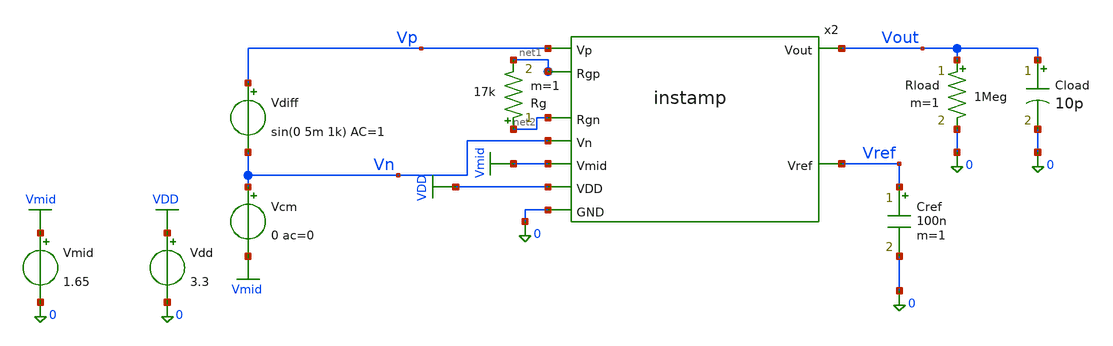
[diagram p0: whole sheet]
** sch_path: xschem/instamp_tb.sch
* Copyright 2021 Stefan Frederik Schippers
* Licensed under the Apache License, Version 2.0 (the "License");
* you may not use this file except in compliance with the License.
* You may obtain a copy of the License at
* https://www.apache.org/licenses/LICENSE-2.0
* Unless required by applicable law or agreed to in writing, software
* distributed under the License is distributed on an "AS IS" BASIS,
* WITHOUT WARRANTIES OR CONDITIONS OF ANY KIND, either express or implied.
* See the License for the specific language governing permissions and
* limitations under the License.
**.subckt instamp_tb
Vdd VDD 0 3.3
Vdiff Vp Vn sin(0 5m 1k) AC=1
Vmid Vmid 0 1.65
Vcm Vn Vmid 0 ac=0
x2 Vn net2 Vp net1 Vmid Vout Vref VDD 0 instamp
Cref Vref 0 100n m=1
Rg net2 net1 17k m=1
Rload Vout 0 1Meg m=1
Cload Vout 0 10p m=1
**** begin user architecture code

** opencircuitdesign pdks install
.lib $::SKYWATER_MODELS/sky130.lib.spice tt



.option wnflag=1
.option savecurrents
.option rshunt=1e12

# if one of these is uncommented, it will
# override the subcircuit in the symbol
# from the cace extracction
#.include ../netlist/rcx/instamp.spice
# from the mag extraction
#.include ../netlist/layout/instamp.spice

.save all
.control
if 0
op
write instamp_tb.raw
endif

set appendwrite
set gnuplot_terminal=png/quit

* write instamp_tb.raw
if 0
* differential gain tran
  destroy all
  foreach val 10k 5k 1k
    alter Rg = $val
    tran 10u 3m 1m
  end
  let Rg10k = tran1.v(vout)
  let Rg5k = tran2.v(vout)
  let Rg1k = tran3.v(vout)
  gnuplot tran Rg10k Rg5k Rg1k
*+ title 'Differential gain'  xlabel 'Time' ylabel 'Volts'
endif

# rise and fall times
if 0
let per=5u
let tstop=$&per*3
let tstep=per/1000
alter Rg=90k
alter @Vdiff[pulse] [ 0 100m $&per 1n 1n $&per $&tstop ]
tran $&tstep $&tstop
plot V(Vp,vmid) V(vout,vmid)
meas tran v_min MIN V(Vout)
meas tran v_pp PP V(Vout)
let v_high=(0.9*v_pp)+v_min
let v_low=(0.1*v_pp)+v_min
meas tran rise_time TRIG v(Vout) VAL='v_low' rise=1 targ v(vout) Val='v_high' RISE=1
let sr=(v_high-v_low)/rise_time
print sr

  gnuplot v_rise_fall V(vp,vmid) V(Vout,vmid)  title 'Rise and Fall Times'  xlabel 'Time (s)' ylabel
+ 'Volts'

endif

if 0
ac dec 100 1 1Meg
let gain = db(V(Vout))
let cutoff_db = vecmax(gain)-3.0
meas ac bw WHEN gain=cutoff_db FALL =1
meas ac max_gain MAX gain
print bw max_gain
endif
* run ac on schematic as drawn
if 1
  destroy all
* differential gain ac
  ac dec 100 1 1Meg
  plot db(v(vout))
endif

* run ac cmrr and psrr sweeps
if 0
  destroy all
* differential gain ac
  alter vdiff ac=1
  alter vcm ac=0
  alter vdd ac=0
  foreach val 10k 5k 1k
    alter Rg = $val
    ac dec 100 1 1Meg
  end
  alter vdiff ac=0
  alter vcm ac=1
  alter vdd ac=0
  foreach val 10k 5k 1k
    alter Rg = $val
    ac dec 100 1 1Meg
  end
  alter vdiff ac=0
  alter vcm ac=0
  alter vdd ac=1
  foreach val 10k 5k 1k
    alter Rg = $val
    ac dec 100 1 1Meg
  end
  alter vdiff ac=0
  alter vcm ac=0
  alter vdd ac=0
  alter vmid ac=1
  foreach val 10k 5k 1k
    alter Rg = $val
    ac dec 100 1 1Meg
  end
  let Rg10k = db(ac1.v(vout))
  let Rg5k = db(ac2.v(vout))
  let Rg1k = db(ac3.v(vout))
  let Rg10k_cm = Rg10k-db(ac4.v(vout))
  let Rg5k_cm = Rg5k-db(ac5.v(vout))
  let Rg1k_cm = Rg1k-db(ac6.v(vout))
  let Rg10k_psh = Rg10k-db(ac7.v(vout))
  let Rg5k_psh = Rg5k-db(ac8.v(vout))
  let Rg1k_psh = Rg1k-db(ac9.v(vout))
  let Rg10k_vmid = Rg10k-db(ac10.v(vout))
  let Rg5k_vmid = Rg5k-db(ac11.v(vout))
  let Rg1k_vmid = Rg1k-db(ac12.v(vout))

  gnuplot ac Rg10k Rg5k Rg1k  title 'Differential gain'  xlabel 'Freq' ylabel 'Gain dB'
  gnuplot cmrr Rg10k_cm Rg5k_cm Rg1k_cm  title 'CMRR'  xlabel 'Freq' ylabel 'Gain dB'
  gnuplot psrr Rg10k_psh Rg5k_psh Rg1k_psh  title 'PSRR'  xlabel 'Freq' ylabel 'Gain dB'
  gnuplot vmid_rej Rg10k_vmid Rg5k_vmid Rg1k_vmid  title 'Vmid Rejection'  xlabel 'Freq' ylabel 'Gain dB'

endif

if 0
* common mode gain
  alter vdiff ac=0
  alter vcm ac=1
  foreach val 90k 5k 1k
    alter Rg = $val
    ac dec 100 1 10Meg
  end

  plot db(ac1.V(Vout)) db(ac2.V(Vout))   db(ac3.V(Vout)) title 'Mag Vout'

* power supply gain
  alter vcm ac=0
  alter vdd ac=1
  foreach val 90k 5k 1k
    alter Rg = $val
    ac dec 100 1 10Meg
  end

  plot db(ac4.V(Vout)) db(ac5.V(Vout))   db(ac6.V(Vout)) title 'Mag Vout'

endif

.endc


**** end user architecture code
**.ends

* expanding   symbol:  instamp.sym # of pins=9
** sym_path: xschem/instamp.sym
** sch_path: xschem/instamp.sch
.subckt instamp Vn Rgn Vp Rgp Vmid Vout Vref VDD GND
*.ipin Vp
*.ipin Vn
*.opin Vout
*.opin Vref
*.ipin Rgp
*.ipin Rgn
*.ipin Vmid
*.ipin GND
*.ipin VDD
XR1 Rgp Vout3 GND sky130_fd_pr__res_high_po_0p35 L=76.36 mult=1 m=1
XR2 Rgn Vout2 GND sky130_fd_pr__res_high_po_0p35 L=76.36 mult=1 m=1
XR3 Vout2 Vn4 GND sky130_fd_pr__res_high_po_0p35 L=51.36 mult=1 m=1
XR4 Vout3 Vp4 GND sky130_fd_pr__res_high_po_0p35 L=51.36 mult=1 m=1
XR5 Vp4 Vout5 GND sky130_fd_pr__res_high_po_0p35 L=51.36 mult=1 m=1
XR6 Vn4 Vout GND sky130_fd_pr__res_high_po_0p35 L=51.36 mult=1 m=1
x6 Vref Vout3 Vp Rgp VDD GND opamp
x2 Vref Vout2 Vn Rgn VDD GND opamp
x3 Vref Vout Vp4 Vn4 VDD GND opamp
x4 Vref Vout5 Vmid Vout5 VDD GND opamp
x1 Vref GND VDD bandgap
.ends


* expanding   symbol:  opamp.sym # of pins=6
** sym_path: xschem/opamp.sym
** sch_path: xschem/opamp.sch
.subckt opamp Vref Vout Vp Vn VDD GND
*.opin Vout
*.ipin Vref
*.ipin Vp
*.ipin Vn
*.ipin GND
*.ipin VDD
XM1 Vg1 Vg1 net1 GND sky130_fd_pr__nfet_g5v0d10v5 L=2 W=3.33 nf=1 ad='int((1 + 1)/2) * 3.33 / 1 * 0.29'
+ as='int((1 + 2)/2) * 3.33 / 1 * 0.29' pd='2*int((1 + 1)/2) * (3.33 / 1 + 0.29)' ps='2*int((1 + 2)/2) * (3.33 / 1 + 0.29)'
+ nrd='0.29 / 3.33 ' nrs='0.29 / 3.33 ' sa=0 sb=0 sd=0 mult=3 m=3
XM2 net1 Vg1 GND GND sky130_fd_pr__nfet_g5v0d10v5 L=5 W=5 nf=1 ad='int((1 + 1)/2) * 5 / 1 * 0.29' as='int((1 + 2)/2) * 5 / 1 * 0.29'
+ pd='2*int((1 + 1)/2) * (5 / 1 + 0.29)' ps='2*int((1 + 2)/2) * (5 / 1 + 0.29)' nrd='0.29 / 5 ' nrs='0.29 / 5 '
+ sa=0 sb=0 sd=0 mult=1 m=1
XM4 net2 Vg1 GND GND sky130_fd_pr__nfet_g5v0d10v5 L=5 W=5 nf=1 ad='int((1 + 1)/2) * 5 / 1 * 0.29' as='int((1 + 2)/2) * 5 / 1 * 0.29'
+ pd='2*int((1 + 1)/2) * (5 / 1 + 0.29)' ps='2*int((1 + 2)/2) * (5 / 1 + 0.29)' nrd='0.29 / 5 ' nrs='0.29 / 5 '
+ sa=0 sb=0 sd=0 mult=1 m=1
XM3 Vg5 Vg1 net2 GND sky130_fd_pr__nfet_g5v0d10v5 L=2 W=3.33 nf=1 ad='int((1 + 1)/2) * 3.33 / 1 * 0.29'
+ as='int((1 + 2)/2) * 3.33 / 1 * 0.29' pd='2*int((1 + 1)/2) * (3.33 / 1 + 0.29)' ps='2*int((1 + 2)/2) * (3.33 / 1 + 0.29)'
+ nrd='0.29 / 3.33 ' nrs='0.29 / 3.33 ' sa=0 sb=0 sd=0 mult=3 m=3
XMr1 net6 Vref GND GND sky130_fd_pr__nfet_g5v0d10v5 L=8 W=5 nf=1 ad='int((1 + 1)/2) * 5 / 1 * 0.29' as='int((1 + 2)/2) * 5 / 1 * 0.29'
+ pd='2*int((1 + 1)/2) * (5 / 1 + 0.29)' ps='2*int((1 + 2)/2) * (5 / 1 + 0.29)' nrd='0.29 / 5 ' nrs='0.29 / 5 '
+ sa=0 sb=0 sd=0 mult=1 m=1
XMr2 VgR2 VgR2 VDD VDD sky130_fd_pr__pfet_g5v0d10v5 L=5 W=4 nf=1 ad='int((1 + 1)/2) * 4 / 1 * 0.29' as='int((1 + 2)/2) * 4 / 1 * 0.29'
+ pd='2*int((1 + 1)/2) * (4 / 1 + 0.29)' ps='2*int((1 + 2)/2) * (4 / 1 + 0.29)' nrd='0.29 / 4 ' nrs='0.29 / 4 '
+ sa=0 sb=0 sd=0 mult=1 m=1
XMr3 Vg1 VgR2 VDD VDD sky130_fd_pr__pfet_g5v0d10v5 L=5 W=4 nf=1 ad='int((1 + 1)/2) * 4 / 1 * 0.29' as='int((1 + 2)/2) * 4 / 1 * 0.29'
+ pd='2*int((1 + 1)/2) * (4 / 1 + 0.29)' ps='2*int((1 + 2)/2) * (4 / 1 + 0.29)' nrd='0.29 / 4 ' nrs='0.29 / 4 '
+ sa=0 sb=0 sd=0 mult=1 m=1
XM32 net3 Vg1 GND GND sky130_fd_pr__nfet_g5v0d10v5 L=5 W=10 nf=1 ad='int((1 + 1)/2) * 10 / 1 * 0.29'
+ as='int((1 + 2)/2) * 10 / 1 * 0.29' pd='2*int((1 + 1)/2) * (10 / 1 + 0.29)' ps='2*int((1 + 2)/2) * (10 / 1 + 0.29)'
+ nrd='0.29 / 10 ' nrs='0.29 / 10 ' sa=0 sb=0 sd=0 mult=1 m=1
XM31 Vs29 Vg1 net3 GND sky130_fd_pr__nfet_g5v0d10v5 L=2 W=6.66 nf=1 ad='int((1 + 1)/2) * 6.66 / 1 * 0.29'
+ as='int((1 + 2)/2) * 6.66 / 1 * 0.29' pd='2*int((1 + 1)/2) * (6.66 / 1 + 0.29)' ps='2*int((1 + 2)/2) * (6.66 / 1 + 0.29)'
+ nrd='0.29 / 6.66 ' nrs='0.29 / 6.66 ' sa=0 sb=0 sd=0 mult=3 m=3
XM15 Vg11 Vg1 Vd10 GND sky130_fd_pr__nfet_g5v0d10v5 L=2 W=14.3 nf=1 ad='int((1 + 1)/2) * 14.3 / 1 * 0.29'
+ as='int((1 + 2)/2) * 14.3 / 1 * 0.29' pd='2*int((1 + 1)/2) * (14.3 / 1 + 0.29)' ps='2*int((1 + 2)/2) * (14.3 / 1 + 0.29)'
+ nrd='0.29 / 14.3 ' nrs='0.29 / 14.3 ' sa=0 sb=0 sd=0 mult=7 m=7
XM16 Vd10 Vg1 GND GND sky130_fd_pr__nfet_g5v0d10v5 L=5 W=10 nf=1 ad='int((1 + 1)/2) * 10 / 1 * 0.29'
+ as='int((1 + 2)/2) * 10 / 1 * 0.29' pd='2*int((1 + 1)/2) * (10 / 1 + 0.29)' ps='2*int((1 + 2)/2) * (10 / 1 + 0.29)'
+ nrd='0.29 / 10 ' nrs='0.29 / 10 ' sa=0 sb=0 sd=0 mult=1 m=1
XM18 Vd9 Vg1 GND GND sky130_fd_pr__nfet_g5v0d10v5 L=5 W=10 nf=1 ad='int((1 + 1)/2) * 10 / 1 * 0.29' as='int((1 + 2)/2) * 10 / 1 * 0.29'
+ pd='2*int((1 + 1)/2) * (10 / 1 + 0.29)' ps='2*int((1 + 2)/2) * (10 / 1 + 0.29)' nrd='0.29 / 10 ' nrs='0.29 / 10 '
+ sa=0 sb=0 sd=0 mult=1 m=1
XM17 Vg28 Vg1 Vd9 GND sky130_fd_pr__nfet_g5v0d10v5 L=2 W=14.3 nf=1 ad='int((1 + 1)/2) * 14.3 / 1 * 0.29'
+ as='int((1 + 2)/2) * 14.3 / 1 * 0.29' pd='2*int((1 + 1)/2) * (14.3 / 1 + 0.29)' ps='2*int((1 + 2)/2) * (14.3 / 1 + 0.29)'
+ nrd='0.29 / 14.3 ' nrs='0.29 / 14.3 ' sa=0 sb=0 sd=0 mult=7 m=7
XM20 Vg22 Vg1 GND GND sky130_fd_pr__nfet_g5v0d10v5 L=5 W=1.5 nf=1 ad='int((1 + 1)/2) * 1.5 / 1 * 0.29'
+ as='int((1 + 2)/2) * 1.5 / 1 * 0.29' pd='2*int((1 + 1)/2) * (1.5 / 1 + 0.29)' ps='2*int((1 + 2)/2) * (1.5 / 1 + 0.29)'
+ nrd='0.29 / 1.5 ' nrs='0.29 / 1.5 ' sa=0 sb=0 sd=0 mult=1 m=1
XM26 Vg26 Vg26 GND GND sky130_fd_pr__nfet_g5v0d10v5 L=0.5 W=5 nf=1 ad='int((1 + 1)/2) * 5 / 1 * 0.29'
+ as='int((1 + 2)/2) * 5 / 1 * 0.29' pd='2*int((1 + 1)/2) * (5 / 1 + 0.29)' ps='2*int((1 + 2)/2) * (5 / 1 + 0.29)'
+ nrd='0.29 / 5 ' nrs='0.29 / 5 ' sa=0 sb=0 sd=0 mult=5 m=5
XM25 Vd24 Vd24 Vg26 GND sky130_fd_pr__nfet_g5v0d10v5 L=0.5 W=5 nf=1 ad='int((1 + 1)/2) * 5 / 1 * 0.29'
+ as='int((1 + 2)/2) * 5 / 1 * 0.29' pd='2*int((1 + 1)/2) * (5 / 1 + 0.29)' ps='2*int((1 + 2)/2) * (5 / 1 + 0.29)'
+ nrd='0.29 / 5 ' nrs='0.29 / 5 ' sa=0 sb=0 sd=0 mult=5 m=5
XM23 Vg27 Vd24 Vg28 GND sky130_fd_pr__nfet_g5v0d10v5 L=0.5 W=10 nf=1 ad='int((1 + 1)/2) * 10 / 1 * 0.29'
+ as='int((1 + 2)/2) * 10 / 1 * 0.29' pd='2*int((1 + 1)/2) * (10 / 1 + 0.29)' ps='2*int((1 + 2)/2) * (10 / 1 + 0.29)'
+ nrd='0.29 / 10 ' nrs='0.29 / 10 ' sa=0 sb=0 sd=0 mult=5 m=5
XM28 Vout Vg28 GND GND sky130_fd_pr__nfet_g5v0d10v5 L=0.5 W=10 nf=1 ad='int((1 + 1)/2) * 10 / 1 * 0.29'
+ as='int((1 + 2)/2) * 10 / 1 * 0.29' pd='2*int((1 + 1)/2) * (10 / 1 + 0.29)' ps='2*int((1 + 2)/2) * (10 / 1 + 0.29)'
+ nrd='0.29 / 10 ' nrs='0.29 / 10 ' sa=0 sb=0 sd=0 mult=15 m=15
XM30 Vd30 Vn Vs29 GND sky130_fd_pr__nfet_g5v0d10v5 L=1.5 W=11.11 nf=1 ad='int((1 + 1)/2) * 11.11 / 1 * 0.29'
+ as='int((1 + 2)/2) * 11.11 / 1 * 0.29' pd='2*int((1 + 1)/2) * (11.11 / 1 + 0.29)' ps='2*int((1 + 2)/2) * (11.11 / 1 + 0.29)'
+ nrd='0.29 / 11.11 ' nrs='0.29 / 11.11 ' sa=0 sb=0 sd=0 mult=9 m=9
XM29 Vd29 Vp Vs29 GND sky130_fd_pr__nfet_g5v0d10v5 L=1.5 W=11.11 nf=1 ad='int((1 + 1)/2) * 11.11 / 1 * 0.29'
+ as='int((1 + 2)/2) * 11.11 / 1 * 0.29' pd='2*int((1 + 1)/2) * (11.11 / 1 + 0.29)' ps='2*int((1 + 2)/2) * (11.11 / 1 + 0.29)'
+ nrd='0.29 / 11.11 ' nrs='0.29 / 11.11 ' sa=0 sb=0 sd=0 mult=9 m=9
XM5 net4 Vg5 VDD VDD sky130_fd_pr__pfet_g5v0d10v5 L=5 W=5 nf=1 ad='int((1 + 1)/2) * 5 / 1 * 0.29' as='int((1 + 2)/2) * 5 / 1 * 0.29'
+ pd='2*int((1 + 1)/2) * (5 / 1 + 0.29)' ps='2*int((1 + 2)/2) * (5 / 1 + 0.29)' nrd='0.29 / 5 ' nrs='0.29 / 5 '
+ sa=0 sb=0 sd=0 mult=3 m=3
XM6 Vg5 Vg5 net4 VDD sky130_fd_pr__pfet_g5v0d10v5 L=2 W=6.6 nf=1 ad='int((1 + 1)/2) * 6.6 / 1 * 0.29'
+ as='int((1 + 2)/2) * 6.6 / 1 * 0.29' pd='2*int((1 + 1)/2) * (6.6 / 1 + 0.29)' ps='2*int((1 + 2)/2) * (6.6 / 1 + 0.29)'
+ nrd='0.29 / 6.6 ' nrs='0.29 / 6.6 ' sa=0 sb=0 sd=0 mult=3 m=3
XM7 net5 Vg5 VDD VDD sky130_fd_pr__pfet_g5v0d10v5 L=5 W=10 nf=1 ad='int((1 + 1)/2) * 10 / 1 * 0.29' as='int((1 + 2)/2) * 10 / 1 * 0.29'
+ pd='2*int((1 + 1)/2) * (10 / 1 + 0.29)' ps='2*int((1 + 2)/2) * (10 / 1 + 0.29)' nrd='0.29 / 10 ' nrs='0.29 / 10 '
+ sa=0 sb=0 sd=0 mult=3 m=3
XM8 Vd8 Vg5 net5 VDD sky130_fd_pr__pfet_g5v0d10v5 L=2 W=13.2 nf=1 ad='int((1 + 1)/2) * 13.2 / 1 * 0.29'
+ as='int((1 + 2)/2) * 13.2 / 1 * 0.29' pd='2*int((1 + 1)/2) * (13.2 / 1 + 0.29)' ps='2*int((1 + 2)/2) * (13.2 / 1 + 0.29)'
+ nrd='0.29 / 13.2 ' nrs='0.29 / 13.2 ' sa=0 sb=0 sd=0 mult=3 m=3
XM09 Vd9 Vp Vd8 Vd8 sky130_fd_pr__pfet_g5v0d10v5 L=1.5 W=22.22 nf=1 ad='int((1 + 1)/2) * 22.22 / 1 * 0.29'
+ as='int((1 + 2)/2) * 22.22 / 1 * 0.29' pd='2*int((1 + 1)/2) * (22.22 / 1 + 0.29)' ps='2*int((1 + 2)/2) * (22.22 / 1 + 0.29)'
+ nrd='0.29 / 22.22 ' nrs='0.29 / 22.22 ' sa=0 sb=0 sd=0 mult=9 m=9
XM010 Vd10 Vn Vd8 Vd8 sky130_fd_pr__pfet_g5v0d10v5 L=1.5 W=22.22 nf=1 ad='int((1 + 1)/2) * 22.22 / 1 * 0.29'
+ as='int((1 + 2)/2) * 22.22 / 1 * 0.29' pd='2*int((1 + 1)/2) * (22.22 / 1 + 0.29)' ps='2*int((1 + 2)/2) * (22.22 / 1 + 0.29)'
+ nrd='0.29 / 22.22 ' nrs='0.29 / 22.22 ' sa=0 sb=0 sd=0 mult=9 m=9
XM13 Vd29 Vg11 VDD VDD sky130_fd_pr__pfet_g5v0d10v5 L=2.5 W=10 nf=1 ad='int((1 + 1)/2) * 10 / 1 * 0.29'
+ as='int((1 + 2)/2) * 10 / 1 * 0.29' pd='2*int((1 + 1)/2) * (10 / 1 + 0.29)' ps='2*int((1 + 2)/2) * (10 / 1 + 0.29)'
+ nrd='0.29 / 10 ' nrs='0.29 / 10 ' sa=0 sb=0 sd=0 mult=5 m=5
XM14 Vg27 Vg11 Vd29 VDD sky130_fd_pr__pfet_g5v0d10v5 L=1 W=10 nf=1 ad='int((1 + 1)/2) * 10 / 1 * 0.29'
+ as='int((1 + 2)/2) * 10 / 1 * 0.29' pd='2*int((1 + 1)/2) * (10 / 1 + 0.29)' ps='2*int((1 + 2)/2) * (10 / 1 + 0.29)'
+ nrd='0.29 / 10 ' nrs='0.29 / 10 ' sa=0 sb=0 sd=0 mult=5 m=5
XM11 Vd30 Vg11 VDD VDD sky130_fd_pr__pfet_g5v0d10v5 L=2.5 W=10 nf=1 ad='int((1 + 1)/2) * 10 / 1 * 0.29'
+ as='int((1 + 2)/2) * 10 / 1 * 0.29' pd='2*int((1 + 1)/2) * (10 / 1 + 0.29)' ps='2*int((1 + 2)/2) * (10 / 1 + 0.29)'
+ nrd='0.29 / 10 ' nrs='0.29 / 10 ' sa=0 sb=0 sd=0 mult=5 m=5
XM12 Vg11 Vg11 Vd30 VDD sky130_fd_pr__pfet_g5v0d10v5 L=1 W=10 nf=1 ad='int((1 + 1)/2) * 10 / 1 * 0.29'
+ as='int((1 + 2)/2) * 10 / 1 * 0.29' pd='2*int((1 + 1)/2) * (10 / 1 + 0.29)' ps='2*int((1 + 2)/2) * (10 / 1 + 0.29)'
+ nrd='0.29 / 10 ' nrs='0.29 / 10 ' sa=0 sb=0 sd=0 mult=5 m=5
XM021 Vg21 Vg21 VDD VDD sky130_fd_pr__pfet_g5v0d10v5 L=0.5 W=15 nf=1 ad='int((1 + 1)/2) * 15 / 1 * 0.29'
+ as='int((1 + 2)/2) * 15 / 1 * 0.29' pd='2*int((1 + 1)/2) * (15 / 1 + 0.29)' ps='2*int((1 + 2)/2) * (15 / 1 + 0.29)'
+ nrd='0.29 / 15 ' nrs='0.29 / 15 ' sa=0 sb=0 sd=0 mult=5 m=5
XM022 Vg22 Vg22 Vg21 VDD sky130_fd_pr__pfet_g5v0d10v5 L=0.5 W=15 nf=1 ad='int((1 + 1)/2) * 15 / 1 * 0.29'
+ as='int((1 + 2)/2) * 15 / 1 * 0.29' pd='2*int((1 + 1)/2) * (15 / 1 + 0.29)' ps='2*int((1 + 2)/2) * (15 / 1 + 0.29)'
+ nrd='0.29 / 15 ' nrs='0.29 / 15 ' sa=0 sb=0 sd=0 mult=5 m=5
XM24 Vd24 Vg5 VDD VDD sky130_fd_pr__pfet_g5v0d10v5 L=5 W=4 nf=1 ad='int((1 + 1)/2) * 4 / 1 * 0.29' as='int((1 + 2)/2) * 4 / 1 * 0.29'
+ pd='2*int((1 + 1)/2) * (4 / 1 + 0.29)' ps='2*int((1 + 2)/2) * (4 / 1 + 0.29)' nrd='0.29 / 4 ' nrs='0.29 / 4 '
+ sa=0 sb=0 sd=0 mult=1 m=1
XM27 Vout Vg27 VDD VDD sky130_fd_pr__pfet_g5v0d10v5 L=0.5 W=15 nf=1 ad='int((1 + 1)/2) * 15 / 1 * 0.29'
+ as='int((1 + 2)/2) * 15 / 1 * 0.29' pd='2*int((1 + 1)/2) * (15 / 1 + 0.29)' ps='2*int((1 + 2)/2) * (15 / 1 + 0.29)'
+ nrd='0.29 / 15 ' nrs='0.29 / 15 ' sa=0 sb=0 sd=0 mult=25 m=25
XM19 Vg28 Vg22 Vg27 VDD sky130_fd_pr__pfet_g5v0d10v5 L=0.5 W=10 nf=1 ad='int((1 + 1)/2) * 10 / 1 * 0.29'
+ as='int((1 + 2)/2) * 10 / 1 * 0.29' pd='2*int((1 + 1)/2) * (10 / 1 + 0.29)' ps='2*int((1 + 2)/2) * (10 / 1 + 0.29)'
+ nrd='0.29 / 10 ' nrs='0.29 / 10 ' sa=0 sb=0 sd=0 mult=15 m=15
Vmeas_Iref VgR2 net6 0
.save i(vmeas_iref)
XC1 Vg27 Vout sky130_fd_pr__cap_mim_m3_1 W=30 L=20 MF=4 m=4
XC2 Vg28 Vout sky130_fd_pr__cap_mim_m3_1 W=30 L=20 MF=4 m=4
.ends


* expanding   symbol:  bandgap.sym # of pins=3
** sym_path: xschem/bandgap.sym
** sch_path: xschem/bandgap.sch
.subckt bandgap Vref GND VDD
*.opin Vref
*.ipin GND
*.ipin VDD
XM4 Vg3 Vg3 GND GND sky130_fd_pr__nfet_g5v0d10v5 L=1 W=20 nf=1 ad='int((1 + 1)/2) * 20 / 1 * 0.29' as='int((1 + 2)/2) * 20 / 1 * 0.29'
+ pd='2*int((1 + 1)/2) * (20 / 1 + 0.29)' ps='2*int((1 + 2)/2) * (20 / 1 + 0.29)' nrd='0.29 / 20 ' nrs='0.29 / 20 '
+ sa=0 sb=0 sd=0 mult=1 m=1
XQ1 GND GND Ve1 sky130_fd_pr__pnp_05v5_W3p40L3p40 m=24
XQ2 GND GND Vg2 sky130_fd_pr__pnp_05v5_W3p40L3p40 m=1
XM1 Vg10 Vg1 net1 net1 sky130_fd_pr__pfet_g5v0d10v5 L=1 W=20 nf=1 ad='int((1 + 1)/2) * 20 / 1 * 0.29'
+ as='int((1 + 2)/2) * 20 / 1 * 0.29' pd='2*int((1 + 1)/2) * (20 / 1 + 0.29)' ps='2*int((1 + 2)/2) * (20 / 1 + 0.29)'
+ nrd='0.29 / 20 ' nrs='0.29 / 20 ' sa=0 sb=0 sd=0 mult=1 m=1
XM2 Vg3 Vg2 net1 net1 sky130_fd_pr__pfet_g5v0d10v5 L=1 W=20 nf=1 ad='int((1 + 1)/2) * 20 / 1 * 0.29'
+ as='int((1 + 2)/2) * 20 / 1 * 0.29' pd='2*int((1 + 1)/2) * (20 / 1 + 0.29)' ps='2*int((1 + 2)/2) * (20 / 1 + 0.29)'
+ nrd='0.29 / 20 ' nrs='0.29 / 20 ' sa=0 sb=0 sd=0 mult=1 m=1
XM11 net1 Vg5 VDD VDD sky130_fd_pr__pfet_g5v0d10v5 L=1 W=1 nf=1 ad='int((1 + 1)/2) * 1 / 1 * 0.29' as='int((1 + 2)/2) * 1 / 1 * 0.29'
+ pd='2*int((1 + 1)/2) * (1 / 1 + 0.29)' ps='2*int((1 + 2)/2) * (1 / 1 + 0.29)' nrd='0.29 / 1 ' nrs='0.29 / 1 '
+ sa=0 sb=0 sd=0 mult=1 m=1
XM3 Vg10 Vg3 GND GND sky130_fd_pr__nfet_g5v0d10v5 L=1 W=20 nf=1 ad='int((1 + 1)/2) * 20 / 1 * 0.29' as='int((1 + 2)/2) * 20 / 1 * 0.29'
+ pd='2*int((1 + 1)/2) * (20 / 1 + 0.29)' ps='2*int((1 + 2)/2) * (20 / 1 + 0.29)' nrd='0.29 / 20 ' nrs='0.29 / 20 '
+ sa=0 sb=0 sd=0 mult=1 m=1
XM10 net2 Vg10 GND GND sky130_fd_pr__nfet_g5v0d10v5 L=1 W=20 nf=1 ad='int((1 + 1)/2) * 20 / 1 * 0.29'
+ as='int((1 + 2)/2) * 20 / 1 * 0.29' pd='2*int((1 + 1)/2) * (20 / 1 + 0.29)' ps='2*int((1 + 2)/2) * (20 / 1 + 0.29)'
+ nrd='0.29 / 20 ' nrs='0.29 / 20 ' sa=0 sb=0 sd=0 mult=1 m=1
XM8 Vg12 Vg5 VDD VDD sky130_fd_pr__pfet_g5v0d10v5 L=1 W=1 nf=1 ad='int((1 + 1)/2) * 1 / 1 * 0.29' as='int((1 + 2)/2) * 1 / 1 * 0.29'
+ pd='2*int((1 + 1)/2) * (1 / 1 + 0.29)' ps='2*int((1 + 2)/2) * (1 / 1 + 0.29)' nrd='0.29 / 1 ' nrs='0.29 / 1 '
+ sa=0 sb=0 sd=0 mult=1 m=1
XM5 Vg5 Vg5 VDD VDD sky130_fd_pr__pfet_g5v0d10v5 L=1 W=1 nf=1 ad='int((1 + 1)/2) * 1 / 1 * 0.29' as='int((1 + 2)/2) * 1 / 1 * 0.29'
+ pd='2*int((1 + 1)/2) * (1 / 1 + 0.29)' ps='2*int((1 + 2)/2) * (1 / 1 + 0.29)' nrd='0.29 / 1 ' nrs='0.29 / 1 '
+ sa=0 sb=0 sd=0 mult=1 m=1
XM12 Vref Vg12 VDD VDD sky130_fd_pr__pfet_g5v0d10v5 L=0.5 W=20 nf=1 ad='int((1 + 1)/2) * 20 / 1 * 0.29'
+ as='int((1 + 2)/2) * 20 / 1 * 0.29' pd='2*int((1 + 1)/2) * (20 / 1 + 0.29)' ps='2*int((1 + 2)/2) * (20 / 1 + 0.29)'
+ nrd='0.29 / 20 ' nrs='0.29 / 20 ' sa=0 sb=0 sd=0 mult=1 m=1
XM9 Vg12 Vref net2 GND sky130_fd_pr__nfet_g5v0d10v5 L=1 W=20 nf=1 ad='int((1 + 1)/2) * 20 / 1 * 0.29'
+ as='int((1 + 2)/2) * 20 / 1 * 0.29' pd='2*int((1 + 1)/2) * (20 / 1 + 0.29)' ps='2*int((1 + 2)/2) * (20 / 1 + 0.29)'
+ nrd='0.29 / 20 ' nrs='0.29 / 20 ' sa=0 sb=0 sd=0 mult=1 m=1
XM7a Vg12 Vg12 net6 GND sky130_fd_pr__nfet_g5v0d10v5 L=10 W=0.5 nf=1 ad='int((1 + 1)/2) * 0.5 / 1 * 0.29'
+ as='int((1 + 2)/2) * 0.5 / 1 * 0.29' pd='2*int((1 + 1)/2) * (0.5 / 1 + 0.29)' ps='2*int((1 + 2)/2) * (0.5 / 1 + 0.29)'
+ nrd='0.29 / 0.5 ' nrs='0.29 / 0.5 ' sa=0 sb=0 sd=0 mult=1 m=1
XM7b net6 Vg12 net5 GND sky130_fd_pr__nfet_g5v0d10v5 L=10 W=0.5 nf=1 ad='int((1 + 1)/2) * 0.5 / 1 * 0.29'
+ as='int((1 + 2)/2) * 0.5 / 1 * 0.29' pd='2*int((1 + 1)/2) * (0.5 / 1 + 0.29)' ps='2*int((1 + 2)/2) * (0.5 / 1 + 0.29)'
+ nrd='0.29 / 0.5 ' nrs='0.29 / 0.5 ' sa=0 sb=0 sd=0 mult=1 m=1
XM7c net5 Vg12 net4 GND sky130_fd_pr__nfet_g5v0d10v5 L=10 W=0.5 nf=1 ad='int((1 + 1)/2) * 0.5 / 1 * 0.29'
+ as='int((1 + 2)/2) * 0.5 / 1 * 0.29' pd='2*int((1 + 1)/2) * (0.5 / 1 + 0.29)' ps='2*int((1 + 2)/2) * (0.5 / 1 + 0.29)'
+ nrd='0.29 / 0.5 ' nrs='0.29 / 0.5 ' sa=0 sb=0 sd=0 mult=1 m=1
XM7d net4 Vg12 net3 GND sky130_fd_pr__nfet_g5v0d10v5 L=10 W=0.5 nf=1 ad='int((1 + 1)/2) * 0.5 / 1 * 0.29'
+ as='int((1 + 2)/2) * 0.5 / 1 * 0.29' pd='2*int((1 + 1)/2) * (0.5 / 1 + 0.29)' ps='2*int((1 + 2)/2) * (0.5 / 1 + 0.29)'
+ nrd='0.29 / 0.5 ' nrs='0.29 / 0.5 ' sa=0 sb=0 sd=0 mult=1 m=1
XM7e net3 Vg12 net11 GND sky130_fd_pr__nfet_g5v0d10v5 L=10 W=0.5 nf=1 ad='int((1 + 1)/2) * 0.5 / 1 * 0.29'
+ as='int((1 + 2)/2) * 0.5 / 1 * 0.29' pd='2*int((1 + 1)/2) * (0.5 / 1 + 0.29)' ps='2*int((1 + 2)/2) * (0.5 / 1 + 0.29)'
+ nrd='0.29 / 0.5 ' nrs='0.29 / 0.5 ' sa=0 sb=0 sd=0 mult=1 m=1
XM6 Vg5 Vref Vs5 GND sky130_fd_pr__nfet_g5v0d10v5 L=1 W=5 nf=1 ad='int((1 + 1)/2) * 5 / 1 * 0.29' as='int((1 + 2)/2) * 5 / 1 * 0.29'
+ pd='2*int((1 + 1)/2) * (5 / 1 + 0.29)' ps='2*int((1 + 2)/2) * (5 / 1 + 0.29)' nrd='0.29 / 5 ' nrs='0.29 / 5 '
+ sa=0 sb=0 sd=0 mult=1 m=1
XR1 Vg2 Vref GND sky130_fd_pr__res_high_po_0p35 L=20.1 mult=1 m=1
XR2 Vg1 Vref GND sky130_fd_pr__res_high_po_0p35 L=20.1 mult=1 m=1
XR4 GND Vs5 GND sky130_fd_pr__res_high_po_0p35 L=49.12 mult=1 m=1
XM7f net11 Vg12 net10 GND sky130_fd_pr__nfet_g5v0d10v5 L=10 W=0.5 nf=1 ad='int((1 + 1)/2) * 0.5 / 1 * 0.29'
+ as='int((1 + 2)/2) * 0.5 / 1 * 0.29' pd='2*int((1 + 1)/2) * (0.5 / 1 + 0.29)' ps='2*int((1 + 2)/2) * (0.5 / 1 + 0.29)'
+ nrd='0.29 / 0.5 ' nrs='0.29 / 0.5 ' sa=0 sb=0 sd=0 mult=1 m=1
XM7g net10 Vg12 net9 GND sky130_fd_pr__nfet_g5v0d10v5 L=10 W=0.5 nf=1 ad='int((1 + 1)/2) * 0.5 / 1 * 0.29'
+ as='int((1 + 2)/2) * 0.5 / 1 * 0.29' pd='2*int((1 + 1)/2) * (0.5 / 1 + 0.29)' ps='2*int((1 + 2)/2) * (0.5 / 1 + 0.29)'
+ nrd='0.29 / 0.5 ' nrs='0.29 / 0.5 ' sa=0 sb=0 sd=0 mult=1 m=1
XM7h net9 Vg12 net8 GND sky130_fd_pr__nfet_g5v0d10v5 L=10 W=0.5 nf=1 ad='int((1 + 1)/2) * 0.5 / 1 * 0.29'
+ as='int((1 + 2)/2) * 0.5 / 1 * 0.29' pd='2*int((1 + 1)/2) * (0.5 / 1 + 0.29)' ps='2*int((1 + 2)/2) * (0.5 / 1 + 0.29)'
+ nrd='0.29 / 0.5 ' nrs='0.29 / 0.5 ' sa=0 sb=0 sd=0 mult=1 m=1
XM7I net8 Vg12 net7 GND sky130_fd_pr__nfet_g5v0d10v5 L=10 W=0.5 nf=1 ad='int((1 + 1)/2) * 0.5 / 1 * 0.29'
+ as='int((1 + 2)/2) * 0.5 / 1 * 0.29' pd='2*int((1 + 1)/2) * (0.5 / 1 + 0.29)' ps='2*int((1 + 2)/2) * (0.5 / 1 + 0.29)'
+ nrd='0.29 / 0.5 ' nrs='0.29 / 0.5 ' sa=0 sb=0 sd=0 mult=1 m=1
XM7J net7 Vg12 GND GND sky130_fd_pr__nfet_g5v0d10v5 L=10 W=0.5 nf=1 ad='int((1 + 1)/2) * 0.5 / 1 * 0.29'
+ as='int((1 + 2)/2) * 0.5 / 1 * 0.29' pd='2*int((1 + 1)/2) * (0.5 / 1 + 0.29)' ps='2*int((1 + 2)/2) * (0.5 / 1 + 0.29)'
+ nrd='0.29 / 0.5 ' nrs='0.29 / 0.5 ' sa=0 sb=0 sd=0 mult=1 m=1
XR3 Ve1 Vg1 GND sky130_fd_pr__res_high_po_0p69 L=6.99 mult=1 m=1
.ends

.GLOBAL VDD
.GLOBAL Vmid
.GLOBAL GND
.end
